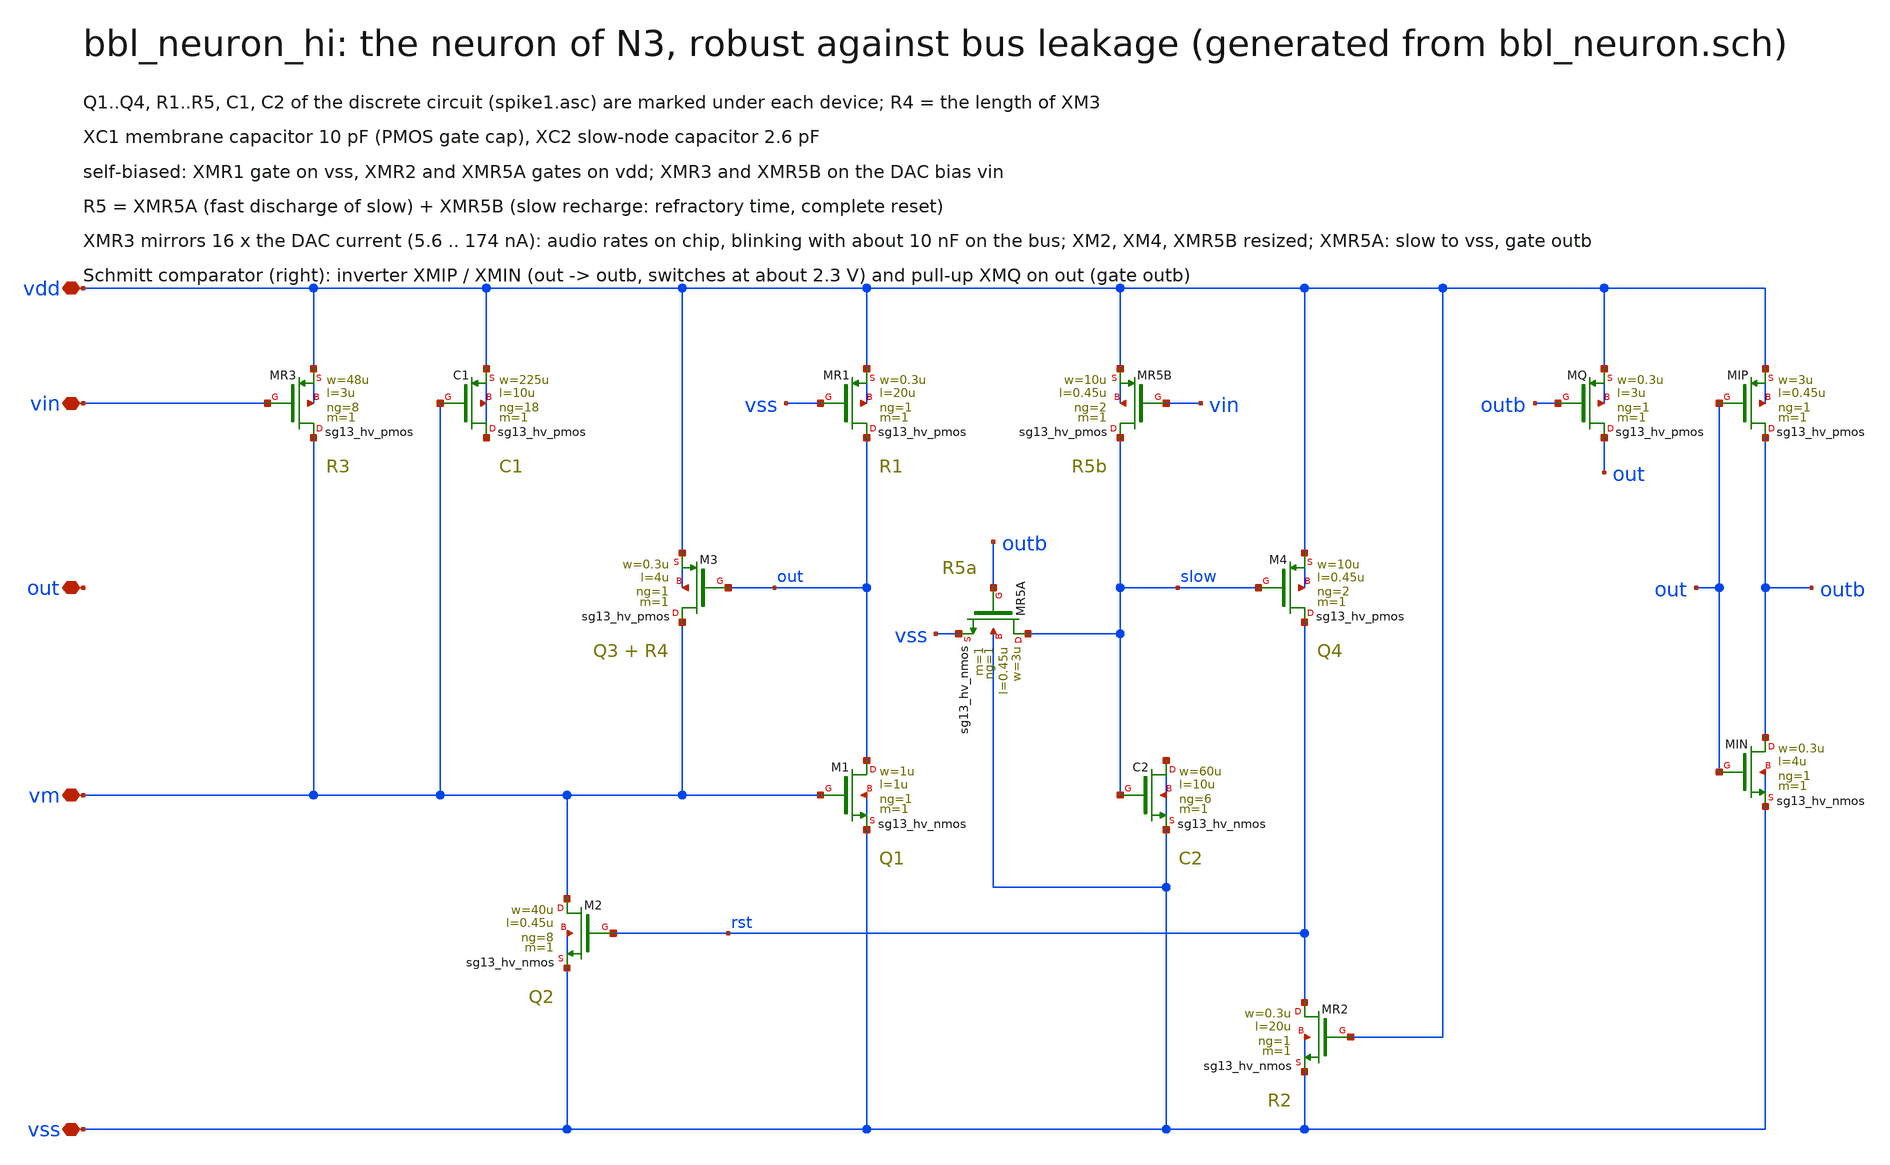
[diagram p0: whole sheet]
** sch_path: schematic/xschem/bbl_neuron_hi.sch
**.subckt bbl_neuron_hi vdd vss vm out vin
*.iopin vdd
*.iopin vss
*.iopin vm
*.iopin out
*.iopin vin
XMR3 vm vin vdd vdd sg13_hv_pmos w=48u l=3u ng=8 m=1 mm_ok=1
XC1 vdd vm vdd vdd sg13_hv_pmos w=225u l=10u ng=18 m=1 mm_ok=1
XM2 vm rst vss vss sg13_hv_nmos w=40u l=0.45u ng=8 m=1 mm_ok=1
XM3 vm out vdd vdd sg13_hv_pmos w=0.3u l=4u ng=1 m=1 mm_ok=1
XMR1 out vss vdd vdd sg13_hv_pmos w=0.3u l=20u ng=1 m=1 mm_ok=1
XM1 out vm vss vss sg13_hv_nmos w=1u l=1u ng=1 m=1 mm_ok=1
XMR5A slow outb vss vss sg13_hv_nmos w=3u l=0.45u ng=1 m=1 mm_ok=1
XMR5B slow vin vdd vdd sg13_hv_pmos w=10u l=0.45u ng=2 m=1 mm_ok=1
XC2 vss slow vss vss sg13_hv_nmos w=60u l=10u ng=6 m=1 mm_ok=1
XM4 rst slow vdd vdd sg13_hv_pmos w=10u l=0.45u ng=2 m=1 mm_ok=1
XMR2 rst vdd vss vss sg13_hv_nmos w=0.3u l=20u ng=1 m=1 mm_ok=1
XMQ out outb vdd vdd sg13_hv_pmos w=0.3u l=3u ng=1 m=1 mm_ok=1
XMIP outb out vdd vdd sg13_hv_pmos w=3u l=0.45u ng=1 m=1 mm_ok=1
XMIN outb out vss vss sg13_hv_nmos w=0.3u l=4u ng=1 m=1 mm_ok=1
**.ends
.end
